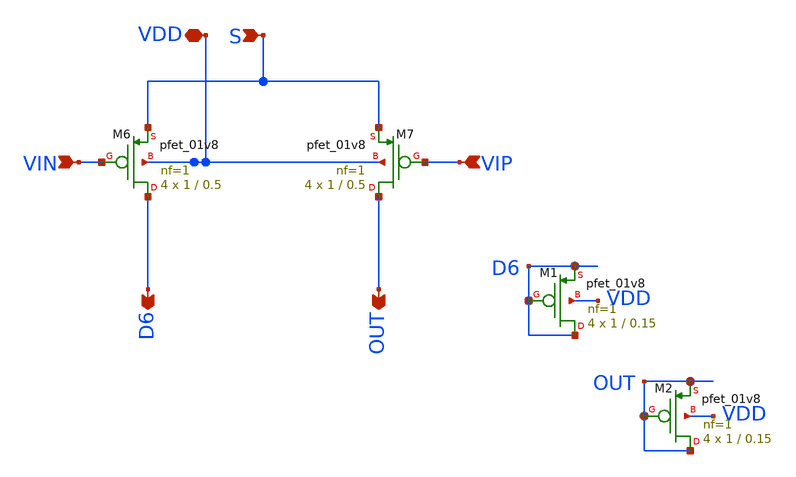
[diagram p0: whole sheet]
** sch_path: opamp/mag/pmosout.sch
**.subckt pmosout VIN VIP S VDD D6 OUT
*.ipin VIN
*.ipin VIP
*.ipin S
*.iopin VDD
*.opin D6
*.opin OUT
XM6 D6 VIN S VDD sky130_fd_pr__pfet_01v8 L=0.5 W=1 nf=1 ad='int((nf+1)/2) * W/nf * 0.29' as='int((nf+2)/2) * W/nf * 0.29'
+ pd='2*int((nf+1)/2) * (W/nf + 0.29)' ps='2*int((nf+2)/2) * (W/nf + 0.29)' nrd='0.29 / W' nrs='0.29 / W'
+ sa=0 sb=0 sd=0 mult=4 m=4
XM7 OUT VIP S VDD sky130_fd_pr__pfet_01v8 L=0.5 W=1 nf=1 ad='int((nf+1)/2) * W/nf * 0.29' as='int((nf+2)/2) * W/nf * 0.29'
+ pd='2*int((nf+1)/2) * (W/nf + 0.29)' ps='2*int((nf+2)/2) * (W/nf + 0.29)' nrd='0.29 / W' nrs='0.29 / W'
+ sa=0 sb=0 sd=0 mult=4 m=4
XM1 D6 D6 D6 VDD sky130_fd_pr__pfet_01v8 L=0.15 W=1 nf=1 ad='int((nf+1)/2) * W/nf * 0.29' as='int((nf+2)/2) * W/nf * 0.29'
+ pd='2*int((nf+1)/2) * (W/nf + 0.29)' ps='2*int((nf+2)/2) * (W/nf + 0.29)' nrd='0.29 / W' nrs='0.29 / W'
+ sa=0 sb=0 sd=0 mult=4 m=4
XM2 OUT OUT OUT VDD sky130_fd_pr__pfet_01v8 L=0.15 W=1 nf=1 ad='int((nf+1)/2) * W/nf * 0.29' as='int((nf+2)/2) * W/nf * 0.29'
+ pd='2*int((nf+1)/2) * (W/nf + 0.29)' ps='2*int((nf+2)/2) * (W/nf + 0.29)' nrd='0.29 / W' nrs='0.29 / W'
+ sa=0 sb=0 sd=0 mult=4 m=4
**.ends
.end
